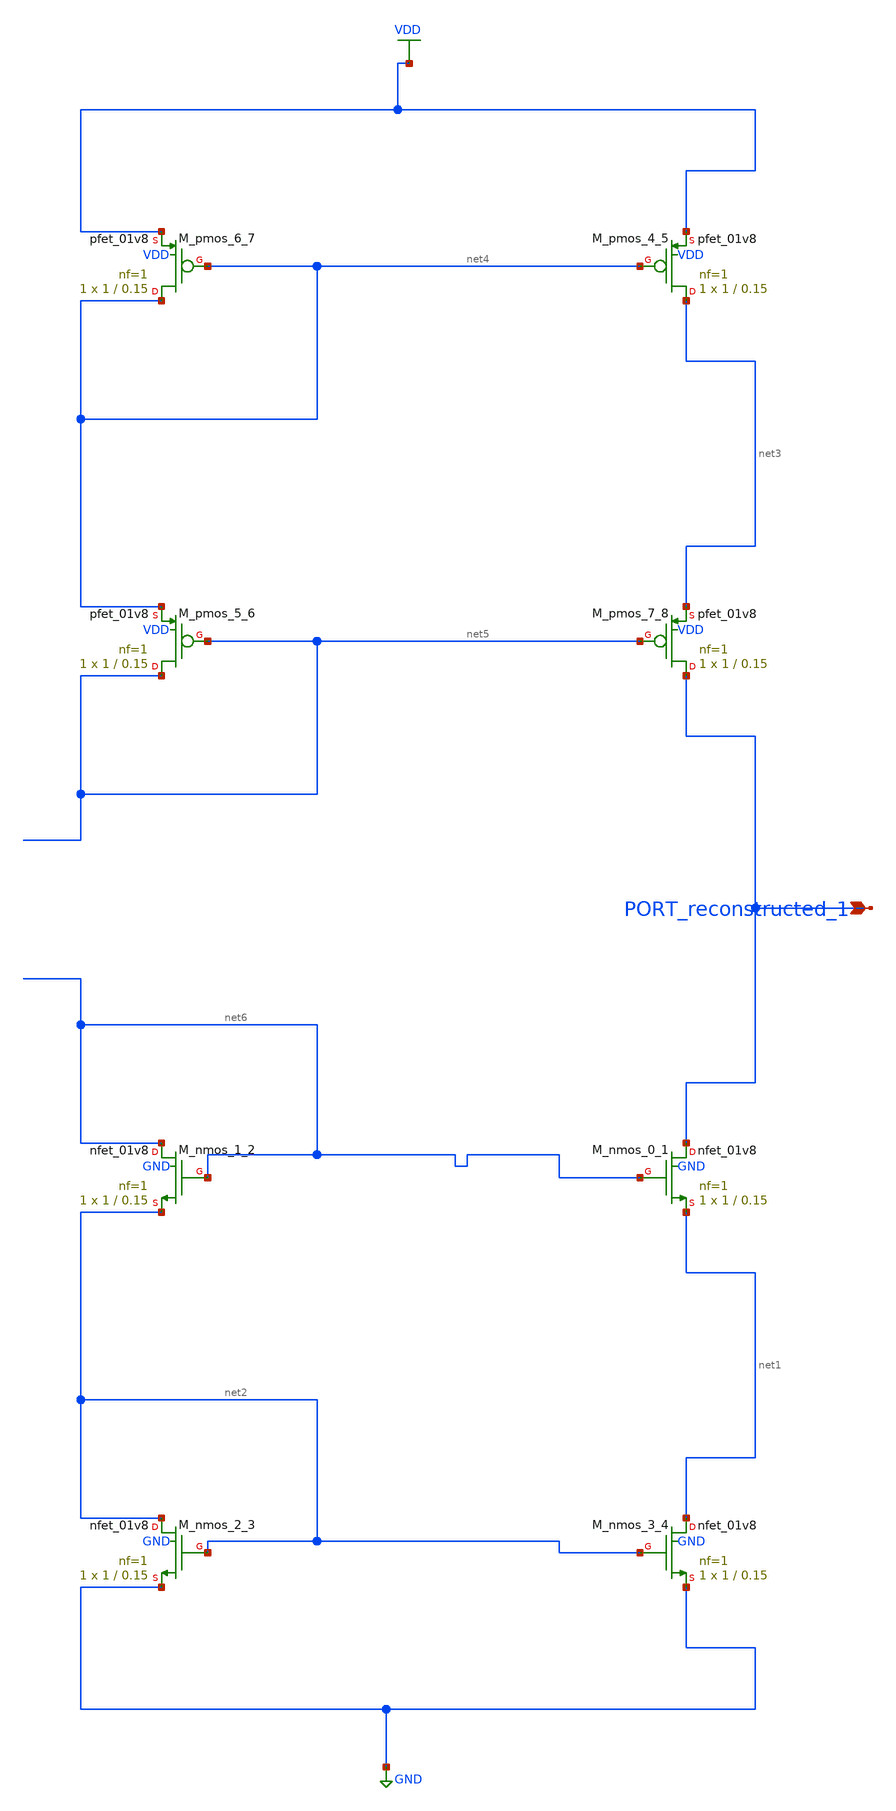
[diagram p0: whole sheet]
** sch_path: schematics/10_1007_s10470-025-02481-2_05_001.sch
**.subckt 10_1007_s10470-025-02481-2_05_001 PORT_reconstructed_1
*.ipin PORT_reconstructed_1
XM_nmos_0_1 PORT_reconstructed_1 net6 net1 GND sky130_fd_pr__nfet_01v8 L=0.15 W=1 nf=1 ad='int((1 + 1)/2) * 1 / 1 * 0.29'
+ as='int((1 + 2)/2) * 1 / 1 * 0.29' pd='2*int((1 + 1)/2) * (1 / 1 + 0.29)' ps='2*int((1 + 2)/2) * (1 / 1 + 0.29)'
+ nrd='0.29 / 1 ' nrs='0.29 / 1 ' sa=0 sb=0 sd=0 mult=1 m=1
XM_nmos_1_2 net6 net6 net2 GND sky130_fd_pr__nfet_01v8 L=0.15 W=1 nf=1 ad='int((1 + 1)/2) * 1 / 1 * 0.29'
+ as='int((1 + 2)/2) * 1 / 1 * 0.29' pd='2*int((1 + 1)/2) * (1 / 1 + 0.29)' ps='2*int((1 + 2)/2) * (1 / 1 + 0.29)'
+ nrd='0.29 / 1 ' nrs='0.29 / 1 ' sa=0 sb=0 sd=0 mult=1 m=1
XM_nmos_2_3 net2 net2 GND GND sky130_fd_pr__nfet_01v8 L=0.15 W=1 nf=1 ad='int((1 + 1)/2) * 1 / 1 * 0.29'
+ as='int((1 + 2)/2) * 1 / 1 * 0.29' pd='2*int((1 + 1)/2) * (1 / 1 + 0.29)' ps='2*int((1 + 2)/2) * (1 / 1 + 0.29)'
+ nrd='0.29 / 1 ' nrs='0.29 / 1 ' sa=0 sb=0 sd=0 mult=1 m=1
XM_nmos_3_4 net1 net2 GND GND sky130_fd_pr__nfet_01v8 L=0.15 W=1 nf=1 ad='int((1 + 1)/2) * 1 / 1 * 0.29'
+ as='int((1 + 2)/2) * 1 / 1 * 0.29' pd='2*int((1 + 1)/2) * (1 / 1 + 0.29)' ps='2*int((1 + 2)/2) * (1 / 1 + 0.29)'
+ nrd='0.29 / 1 ' nrs='0.29 / 1 ' sa=0 sb=0 sd=0 mult=1 m=1
XM_pmos_4_5 net3 net4 VDD VDD sky130_fd_pr__pfet_01v8 L=0.15 W=1 nf=1 ad='int((1 + 1)/2) * 1 / 1 * 0.29'
+ as='int((1 + 2)/2) * 1 / 1 * 0.29' pd='2*int((1 + 1)/2) * (1 / 1 + 0.29)' ps='2*int((1 + 2)/2) * (1 / 1 + 0.29)'
+ nrd='0.29 / 1 ' nrs='0.29 / 1 ' sa=0 sb=0 sd=0 mult=1 m=1
XM_pmos_5_6 net5 net5 net4 VDD sky130_fd_pr__pfet_01v8 L=0.15 W=1 nf=1 ad='int((1 + 1)/2) * 1 / 1 * 0.29'
+ as='int((1 + 2)/2) * 1 / 1 * 0.29' pd='2*int((1 + 1)/2) * (1 / 1 + 0.29)' ps='2*int((1 + 2)/2) * (1 / 1 + 0.29)'
+ nrd='0.29 / 1 ' nrs='0.29 / 1 ' sa=0 sb=0 sd=0 mult=1 m=1
XM_pmos_6_7 net4 net4 VDD VDD sky130_fd_pr__pfet_01v8 L=0.15 W=1 nf=1 ad='int((1 + 1)/2) * 1 / 1 * 0.29'
+ as='int((1 + 2)/2) * 1 / 1 * 0.29' pd='2*int((1 + 1)/2) * (1 / 1 + 0.29)' ps='2*int((1 + 2)/2) * (1 / 1 + 0.29)'
+ nrd='0.29 / 1 ' nrs='0.29 / 1 ' sa=0 sb=0 sd=0 mult=1 m=1
XM_pmos_7_8 PORT_reconstructed_1 net5 net3 VDD sky130_fd_pr__pfet_01v8 L=0.15 W=1 nf=1 ad='int((1 + 1)/2) * 1 / 1 * 0.29'
+ as='int((1 + 2)/2) * 1 / 1 * 0.29' pd='2*int((1 + 1)/2) * (1 / 1 + 0.29)' ps='2*int((1 + 2)/2) * (1 / 1 + 0.29)'
+ nrd='0.29 / 1 ' nrs='0.29 / 1 ' sa=0 sb=0 sd=0 mult=1 m=1
**.ends
.GLOBAL GND
.GLOBAL VDD
.end
